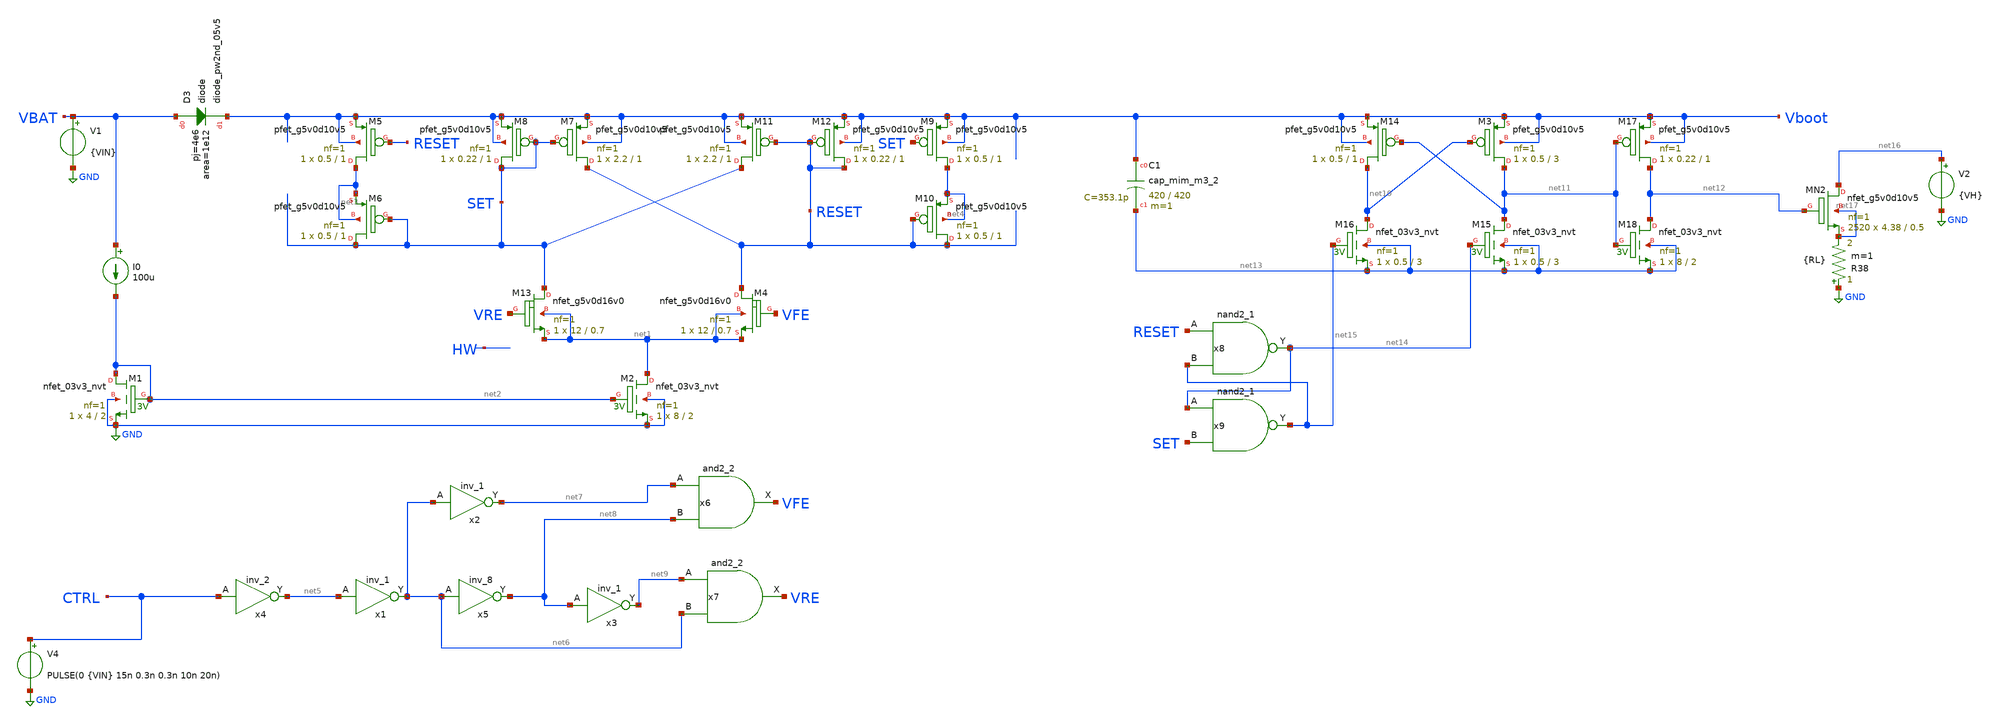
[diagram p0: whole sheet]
** sch_path: LS_boot_20230921/sch/LS_boot_jm.sch
**.subckt LS_boot_jm
XM1 net2 net2 GND GND sky130_fd_pr__nfet_03v3_nvt L=2 W=4 nf=1 ad='int((nf+1)/2) * W/nf * 0.29' as='int((nf+2)/2) * W/nf * 0.29'
+ pd='2*int((nf+1)/2) * (W/nf + 0.29)' ps='2*int((nf+2)/2) * (W/nf + 0.29)' nrd='0.29 / W' nrs='0.29 / W'
+ sa=0 sb=0 sd=0 mult=1 m=1
XM2 net1 net2 GND GND sky130_fd_pr__nfet_03v3_nvt L=2 W=8 nf=1 ad='int((nf+1)/2) * W/nf * 0.29' as='int((nf+2)/2) * W/nf * 0.29'
+ pd='2*int((nf+1)/2) * (W/nf + 0.29)' ps='2*int((nf+2)/2) * (W/nf + 0.29)' nrd='0.29 / W' nrs='0.29 / W'
+ sa=0 sb=0 sd=0 mult=1 m=1
XM5 net3 RESET Vboot Vboot sky130_fd_pr__pfet_g5v0d10v5 L=1 W=0.5 nf=1 ad='int((nf+1)/2) * W/nf * 0.29'
+ as='int((nf+2)/2) * W/nf * 0.29' pd='2*int((nf+1)/2) * (W/nf + 0.29)' ps='2*int((nf+2)/2) * (W/nf + 0.29)'
+ nrd='0.29 / W' nrs='0.29 / W' sa=0 sb=0 sd=0 mult=1 m=1
XM6 SET SET net3 net3 sky130_fd_pr__pfet_g5v0d10v5 L=1 W=0.5 nf=1 ad='int((nf+1)/2) * W/nf * 0.29' as='int((nf+2)/2) * W/nf * 0.29'
+ pd='2*int((nf+1)/2) * (W/nf + 0.29)' ps='2*int((nf+2)/2) * (W/nf + 0.29)' nrd='0.29 / W' nrs='0.29 / W'
+ sa=0 sb=0 sd=0 mult=1 m=1
XM7 RESET SET Vboot Vboot sky130_fd_pr__pfet_g5v0d10v5 L=1 W=2.2 nf=1 ad='int((nf+1)/2) * W/nf * 0.29'
+ as='int((nf+2)/2) * W/nf * 0.29' pd='2*int((nf+1)/2) * (W/nf + 0.29)' ps='2*int((nf+2)/2) * (W/nf + 0.29)'
+ nrd='0.29 / W' nrs='0.29 / W' sa=0 sb=0 sd=0 mult=1 m=1
XM8 SET SET Vboot Vboot sky130_fd_pr__pfet_g5v0d10v5 L=1 W=0.22 nf=1 ad='int((nf+1)/2) * W/nf * 0.29'
+ as='int((nf+2)/2) * W/nf * 0.29' pd='2*int((nf+1)/2) * (W/nf + 0.29)' ps='2*int((nf+2)/2) * (W/nf + 0.29)'
+ nrd='0.29 / W' nrs='0.29 / W' sa=0 sb=0 sd=0 mult=1 m=1
XM9 net4 SET Vboot Vboot sky130_fd_pr__pfet_g5v0d10v5 L=1 W=0.5 nf=1 ad='int((nf+1)/2) * W/nf * 0.29'
+ as='int((nf+2)/2) * W/nf * 0.29' pd='2*int((nf+1)/2) * (W/nf + 0.29)' ps='2*int((nf+2)/2) * (W/nf + 0.29)'
+ nrd='0.29 / W' nrs='0.29 / W' sa=0 sb=0 sd=0 mult=1 m=1
XM10 RESET RESET net4 net4 sky130_fd_pr__pfet_g5v0d10v5 L=1 W=0.5 nf=1 ad='int((nf+1)/2) * W/nf * 0.29'
+ as='int((nf+2)/2) * W/nf * 0.29' pd='2*int((nf+1)/2) * (W/nf + 0.29)' ps='2*int((nf+2)/2) * (W/nf + 0.29)'
+ nrd='0.29 / W' nrs='0.29 / W' sa=0 sb=0 sd=0 mult=1 m=1
XM11 SET RESET Vboot Vboot sky130_fd_pr__pfet_g5v0d10v5 L=1 W=2.2 nf=1 ad='int((nf+1)/2) * W/nf * 0.29'
+ as='int((nf+2)/2) * W/nf * 0.29' pd='2*int((nf+1)/2) * (W/nf + 0.29)' ps='2*int((nf+2)/2) * (W/nf + 0.29)'
+ nrd='0.29 / W' nrs='0.29 / W' sa=0 sb=0 sd=0 mult=1 m=1
XM12 RESET RESET Vboot Vboot sky130_fd_pr__pfet_g5v0d10v5 L=1 W=0.22 nf=1 ad='int((nf+1)/2) * W/nf * 0.29'
+ as='int((nf+2)/2) * W/nf * 0.29' pd='2*int((nf+1)/2) * (W/nf + 0.29)' ps='2*int((nf+2)/2) * (W/nf + 0.29)'
+ nrd='0.29 / W' nrs='0.29 / W' sa=0 sb=0 sd=0 mult=1 m=1
XM4 RESET VFE net1 net1 sky130_fd_pr__nfet_g5v0d16v0 L=0.7 W=12 nf=1 ad='int((nf+1)/2) * W/nf * 0.29'
+ as='int((nf+2)/2) * W/nf * 0.29' pd='2*int((nf+1)/2) * (W/nf + 0.29)' ps='2*int((nf+2)/2) * (W/nf + 0.29)'
+ nrd='0.29 / W' nrs='0.29 / W' sa=0 sb=0 sd=0 mult=1 m=1
XD3 VBAT Vboot sky130_fd_pr__diode_pw2nd_05v5 area=1e12 pj=4e6
I0 VBAT net2 100u
x1 net5 VGND VNB VPB VPWR net6 sky130_fd_sc_hd__inv_1
x2 net6 VGND VNB VPB VPWR net7 sky130_fd_sc_hd__inv_1
x3 net8 VGND VNB VPB VPWR net9 sky130_fd_sc_hd__inv_1
x4 CTRL VGND VNB VPB VPWR net5 sky130_fd_sc_hd__inv_2
x5 net6 VGND VNB VPB VPWR net8 sky130_fd_sc_hd__inv_8
x6 net7 net8 VGND VNB VPB VPWR VFE sky130_fd_sc_hd__and2_2
x7 net9 net6 VGND VNB VPB VPWR VRE sky130_fd_sc_hd__and2_2
XM13 SET VRE net1 net1 sky130_fd_pr__nfet_g5v0d16v0 L=0.7 W=12 nf=1 ad='int((nf+1)/2) * W/nf * 0.29'
+ as='int((nf+2)/2) * W/nf * 0.29' pd='2*int((nf+1)/2) * (W/nf + 0.29)' ps='2*int((nf+2)/2) * (W/nf + 0.29)'
+ nrd='0.29 / W' nrs='0.29 / W' sa=0 sb=0 sd=0 mult=1 m=1
XC1 Vboot net13 sky130_fd_pr__cap_mim_m3_2 W=420 L=420 MF=1 m=1
XM3 net11 net10 Vboot Vboot sky130_fd_pr__pfet_g5v0d10v5 L=3 W=0.5 nf=1 ad='int((nf+1)/2) * W/nf * 0.29'
+ as='int((nf+2)/2) * W/nf * 0.29' pd='2*int((nf+1)/2) * (W/nf + 0.29)' ps='2*int((nf+2)/2) * (W/nf + 0.29)'
+ nrd='0.29 / W' nrs='0.29 / W' sa=0 sb=0 sd=0 mult=1 m=1
XM14 net10 net11 Vboot Vboot sky130_fd_pr__pfet_g5v0d10v5 L=1 W=0.5 nf=1 ad='int((nf+1)/2) * W/nf * 0.29'
+ as='int((nf+2)/2) * W/nf * 0.29' pd='2*int((nf+1)/2) * (W/nf + 0.29)' ps='2*int((nf+2)/2) * (W/nf + 0.29)'
+ nrd='0.29 / W' nrs='0.29 / W' sa=0 sb=0 sd=0 mult=1 m=1
XM15 net11 net14 net13 net13 sky130_fd_pr__nfet_03v3_nvt L=3 W=0.5 nf=1 ad='int((nf+1)/2) * W/nf * 0.29'
+ as='int((nf+2)/2) * W/nf * 0.29' pd='2*int((nf+1)/2) * (W/nf + 0.29)' ps='2*int((nf+2)/2) * (W/nf + 0.29)'
+ nrd='0.29 / W' nrs='0.29 / W' sa=0 sb=0 sd=0 mult=1 m=1
XM16 net10 net15 net13 net13 sky130_fd_pr__nfet_03v3_nvt L=3 W=0.5 nf=1 ad='int((nf+1)/2) * W/nf * 0.29'
+ as='int((nf+2)/2) * W/nf * 0.29' pd='2*int((nf+1)/2) * (W/nf + 0.29)' ps='2*int((nf+2)/2) * (W/nf + 0.29)'
+ nrd='0.29 / W' nrs='0.29 / W' sa=0 sb=0 sd=0 mult=1 m=1
XM17 net12 net11 Vboot Vboot sky130_fd_pr__pfet_g5v0d10v5 L=1 W=0.22 nf=1 ad='int((nf+1)/2) * W/nf * 0.29'
+ as='int((nf+2)/2) * W/nf * 0.29' pd='2*int((nf+1)/2) * (W/nf + 0.29)' ps='2*int((nf+2)/2) * (W/nf + 0.29)'
+ nrd='0.29 / W' nrs='0.29 / W' sa=0 sb=0 sd=0 mult=1 m=1
XM18 net12 net11 net13 net13 sky130_fd_pr__nfet_03v3_nvt L=2 W=8 nf=1 ad='int((nf+1)/2) * W/nf * 0.29'
+ as='int((nf+2)/2) * W/nf * 0.29' pd='2*int((nf+1)/2) * (W/nf + 0.29)' ps='2*int((nf+2)/2) * (W/nf + 0.29)'
+ nrd='0.29 / W' nrs='0.29 / W' sa=0 sb=0 sd=0 mult=1 m=1
x8 RESET net15 VGND VNB VPB VPWR net14 sky130_fd_sc_hd__nand2_1
x9 net14 SET VGND VNB VPB VPWR net15 sky130_fd_sc_hd__nand2_1
V4 CTRL GND PULSE(0 {VIN} 15n 0.3n 0.3n 10n 20n)
V1 VBAT GND {VIN}
XMN2 net16 net12 net17 net17 sky130_fd_pr__nfet_g5v0d10v5 L=0.5 W=4.38 nf=1 ad='int((nf+1)/2) * W/nf * 0.29'
+ as='int((nf+2)/2) * W/nf * 0.29' pd='2*int((nf+1)/2) * (W/nf + 0.29)' ps='2*int((nf+2)/2) * (W/nf + 0.29)'
+ nrd='0.29 / W' nrs='0.29 / W' sa=0 sb=0 sd=0 mult=2520 m=2520
V2 net16 GND {VH}
R38 GND net17 {RL} m=1
**** begin user architecture code


.param VIN = 3.3
.param VH = 12
.param RL = 50
.option scale=1e-6
*.option temp=70
.ic v(V_CFTOP) = VIN/2
.ic v(vout)=0
.ic v(V_CFBOT) = 0
*.probe vd(MP2:G:S)

.param mc_mm_switch=0
*.lib /usr/share/pdk/sky130A/libs.tech/ngspice/sky130.lib.spice ss
*.lib /foss/pdk/sky130A/libs.tech/ngspice/sky130.lib.spice TT
.lib /foss/pdks/sky130A/libs.tech/ngspice/sky130.lib.spice TT
*.include $::SKYWATER_STDCELLS/sky130_fd_sc_hd.spice
.include /foss/pdks/sky130A/libs.ref/sky130_fd_sc_hd/spice/sky130_fd_sc_hd.spice
*.include /usr/share/pdk/sky130A/libs.ref/sky130_fd_sc_hvl/spice/sky130_fd_sc_hvl.spice
*.include /home/jorge/Documents/Postdoc/share/pdk/sky130A/libs.ref/sky130_fd_sc_hvl/spice/sky130_fd_sc_hvl.spice
.options savecurrents
.control
save all
tran 100n 2u
write LS_BOOT.raw
.endc


**** end user architecture code
**.ends
.GLOBAL GND
.end
